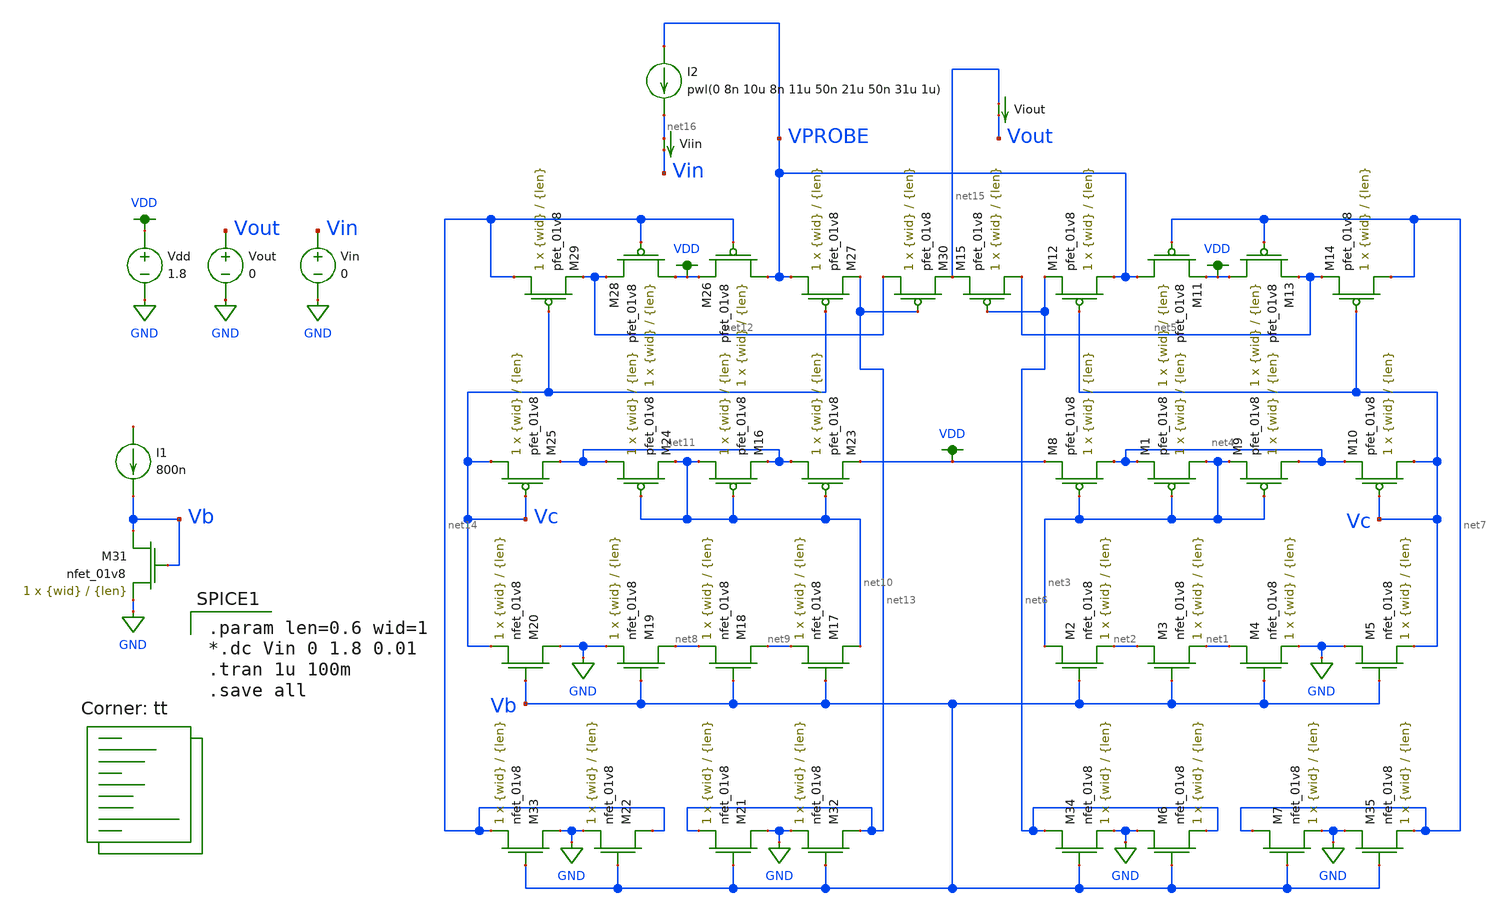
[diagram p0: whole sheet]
** sch_path: mp3/mirror_lvs_tb.sch
**.subckt mirror_lvs_tb
XM1 net3 net3 net4 VDD sky130_fd_pr__pfet_01v8 L={len} W={wid} nf=1 ad='int((nf+1)/2) * W/nf * 0.29'
+ as='int((nf+2)/2) * W/nf * 0.29' pd='2*int((nf+1)/2) * (W/nf + 0.29)' ps='2*int((nf+2)/2) * (W/nf + 0.29)'
+ nrd='0.29 / W' nrs='0.29 / W' sa=0 sb=0 sd=0 mult=1 m=1
XM2 net3 Vb net2 GND sky130_fd_pr__nfet_01v8 L={len} W={wid} nf=1 ad='int((nf+1)/2) * W/nf * 0.29' as='int((nf+2)/2) * W/nf * 0.29'
+ pd='2*int((nf+1)/2) * (W/nf + 0.29)' ps='2*int((nf+2)/2) * (W/nf + 0.29)' nrd='0.29 / W' nrs='0.29 / W'
+ sa=0 sb=0 sd=0 mult=1 m=1
XM3 net2 Vb net1 GND sky130_fd_pr__nfet_01v8 L={len} W={wid} nf=1 ad='int((nf+1)/2) * W/nf * 0.29' as='int((nf+2)/2) * W/nf * 0.29'
+ pd='2*int((nf+1)/2) * (W/nf + 0.29)' ps='2*int((nf+2)/2) * (W/nf + 0.29)' nrd='0.29 / W' nrs='0.29 / W'
+ sa=0 sb=0 sd=0 mult=1 m=1
XM4 net1 Vb GND GND sky130_fd_pr__nfet_01v8 L={len} W={wid} nf=1 ad='int((nf+1)/2) * W/nf * 0.29' as='int((nf+2)/2) * W/nf * 0.29'
+ pd='2*int((nf+1)/2) * (W/nf + 0.29)' ps='2*int((nf+2)/2) * (W/nf + 0.29)' nrd='0.29 / W' nrs='0.29 / W'
+ sa=0 sb=0 sd=0 mult=1 m=1
XM5 GND Vb Vc GND sky130_fd_pr__nfet_01v8 L={len} W={wid} nf=1 ad='int((nf+1)/2) * W/nf * 0.29' as='int((nf+2)/2) * W/nf * 0.29'
+ pd='2*int((nf+1)/2) * (W/nf + 0.29)' ps='2*int((nf+2)/2) * (W/nf + 0.29)' nrd='0.29 / W' nrs='0.29 / W'
+ sa=0 sb=0 sd=0 mult=1 m=1
XM8 net4 net3 VDD VDD sky130_fd_pr__pfet_01v8 L={len} W={wid} nf=1 ad='int((nf+1)/2) * W/nf * 0.29' as='int((nf+2)/2) * W/nf * 0.29'
+ pd='2*int((nf+1)/2) * (W/nf + 0.29)' ps='2*int((nf+2)/2) * (W/nf + 0.29)' nrd='0.29 / W' nrs='0.29 / W'
+ sa=0 sb=0 sd=0 mult=1 m=1
XM9 net4 net3 net3 VDD sky130_fd_pr__pfet_01v8 L={len} W={wid} nf=1 ad='int((nf+1)/2) * W/nf * 0.29'
+ as='int((nf+2)/2) * W/nf * 0.29' pd='2*int((nf+1)/2) * (W/nf + 0.29)' ps='2*int((nf+2)/2) * (W/nf + 0.29)'
+ nrd='0.29 / W' nrs='0.29 / W' sa=0 sb=0 sd=0 mult=1 m=1
XM10 Vc Vc net4 VDD sky130_fd_pr__pfet_01v8 L={len} W={wid} nf=1 ad='int((nf+1)/2) * W/nf * 0.29' as='int((nf+2)/2) * W/nf * 0.29'
+ pd='2*int((nf+1)/2) * (W/nf + 0.29)' ps='2*int((nf+2)/2) * (W/nf + 0.29)' nrd='0.29 / W' nrs='0.29 / W'
+ sa=0 sb=0 sd=0 mult=1 m=1
XM11 VPROBE net7 VDD VDD sky130_fd_pr__pfet_01v8 L={len} W={wid} nf=1 ad='int((nf+1)/2) * W/nf * 0.29'
+ as='int((nf+2)/2) * W/nf * 0.29' pd='2*int((nf+1)/2) * (W/nf + 0.29)' ps='2*int((nf+2)/2) * (W/nf + 0.29)'
+ nrd='0.29 / W' nrs='0.29 / W' sa=0 sb=0 sd=0 mult=1 m=1
XM12 VPROBE Vc net6 VDD sky130_fd_pr__pfet_01v8 L={len} W={wid} nf=1 ad='int((nf+1)/2) * W/nf * 0.29'
+ as='int((nf+2)/2) * W/nf * 0.29' pd='2*int((nf+1)/2) * (W/nf + 0.29)' ps='2*int((nf+2)/2) * (W/nf + 0.29)'
+ nrd='0.29 / W' nrs='0.29 / W' sa=0 sb=0 sd=0 mult=1 m=1
XM13 VDD net7 net5 VDD sky130_fd_pr__pfet_01v8 L={len} W={wid} nf=1 ad='int((nf+1)/2) * W/nf * 0.29'
+ as='int((nf+2)/2) * W/nf * 0.29' pd='2*int((nf+1)/2) * (W/nf + 0.29)' ps='2*int((nf+2)/2) * (W/nf + 0.29)'
+ nrd='0.29 / W' nrs='0.29 / W' sa=0 sb=0 sd=0 mult=1 m=1
XM14 net7 Vc net5 VDD sky130_fd_pr__pfet_01v8 L={len} W={wid} nf=1 ad='int((nf+1)/2) * W/nf * 0.29' as='int((nf+2)/2) * W/nf * 0.29'
+ pd='2*int((nf+1)/2) * (W/nf + 0.29)' ps='2*int((nf+2)/2) * (W/nf + 0.29)' nrd='0.29 / W' nrs='0.29 / W'
+ sa=0 sb=0 sd=0 mult=1 m=1
XM15 net5 net6 net15 VDD sky130_fd_pr__pfet_01v8 L={len} W={wid} nf=1 ad='int((nf+1)/2) * W/nf * 0.29'
+ as='int((nf+2)/2) * W/nf * 0.29' pd='2*int((nf+1)/2) * (W/nf + 0.29)' ps='2*int((nf+2)/2) * (W/nf + 0.29)'
+ nrd='0.29 / W' nrs='0.29 / W' sa=0 sb=0 sd=0 mult=1 m=1
XM16 net10 net10 net11 VDD sky130_fd_pr__pfet_01v8 L={len} W={wid} nf=1 ad='int((nf+1)/2) * W/nf * 0.29'
+ as='int((nf+2)/2) * W/nf * 0.29' pd='2*int((nf+1)/2) * (W/nf + 0.29)' ps='2*int((nf+2)/2) * (W/nf + 0.29)'
+ nrd='0.29 / W' nrs='0.29 / W' sa=0 sb=0 sd=0 mult=1 m=1
XM17 net10 Vb net9 GND sky130_fd_pr__nfet_01v8 L={len} W={wid} nf=1 ad='int((nf+1)/2) * W/nf * 0.29'
+ as='int((nf+2)/2) * W/nf * 0.29' pd='2*int((nf+1)/2) * (W/nf + 0.29)' ps='2*int((nf+2)/2) * (W/nf + 0.29)'
+ nrd='0.29 / W' nrs='0.29 / W' sa=0 sb=0 sd=0 mult=1 m=1
XM18 net9 Vb net8 GND sky130_fd_pr__nfet_01v8 L={len} W={wid} nf=1 ad='int((nf+1)/2) * W/nf * 0.29' as='int((nf+2)/2) * W/nf * 0.29'
+ pd='2*int((nf+1)/2) * (W/nf + 0.29)' ps='2*int((nf+2)/2) * (W/nf + 0.29)' nrd='0.29 / W' nrs='0.29 / W'
+ sa=0 sb=0 sd=0 mult=1 m=1
XM19 net8 Vb GND GND sky130_fd_pr__nfet_01v8 L={len} W={wid} nf=1 ad='int((nf+1)/2) * W/nf * 0.29' as='int((nf+2)/2) * W/nf * 0.29'
+ pd='2*int((nf+1)/2) * (W/nf + 0.29)' ps='2*int((nf+2)/2) * (W/nf + 0.29)' nrd='0.29 / W' nrs='0.29 / W'
+ sa=0 sb=0 sd=0 mult=1 m=1
XM20 GND Vb Vc GND sky130_fd_pr__nfet_01v8 L={len} W={wid} nf=1 ad='int((nf+1)/2) * W/nf * 0.29' as='int((nf+2)/2) * W/nf * 0.29'
+ pd='2*int((nf+1)/2) * (W/nf + 0.29)' ps='2*int((nf+2)/2) * (W/nf + 0.29)' nrd='0.29 / W' nrs='0.29 / W'
+ sa=0 sb=0 sd=0 mult=1 m=1
XM21 GND Vb net13 GND sky130_fd_pr__nfet_01v8 L={len} W={wid} nf=1 ad='int((nf+1)/2) * W/nf * 0.29' as='int((nf+2)/2) * W/nf * 0.29'
+ pd='2*int((nf+1)/2) * (W/nf + 0.29)' ps='2*int((nf+2)/2) * (W/nf + 0.29)' nrd='0.29 / W' nrs='0.29 / W'
+ sa=0 sb=0 sd=0 mult=1 m=1
XM22 net14 Vb GND GND sky130_fd_pr__nfet_01v8 L={len} W={wid} nf=1 ad='int((nf+1)/2) * W/nf * 0.29' as='int((nf+2)/2) * W/nf * 0.29'
+ pd='2*int((nf+1)/2) * (W/nf + 0.29)' ps='2*int((nf+2)/2) * (W/nf + 0.29)' nrd='0.29 / W' nrs='0.29 / W'
+ sa=0 sb=0 sd=0 mult=1 m=1
XM23 net11 net10 VDD VDD sky130_fd_pr__pfet_01v8 L={len} W={wid} nf=1 ad='int((nf+1)/2) * W/nf * 0.29'
+ as='int((nf+2)/2) * W/nf * 0.29' pd='2*int((nf+1)/2) * (W/nf + 0.29)' ps='2*int((nf+2)/2) * (W/nf + 0.29)'
+ nrd='0.29 / W' nrs='0.29 / W' sa=0 sb=0 sd=0 mult=1 m=1
XM24 net11 net10 net10 VDD sky130_fd_pr__pfet_01v8 L={len} W={wid} nf=1 ad='int((nf+1)/2) * W/nf * 0.29'
+ as='int((nf+2)/2) * W/nf * 0.29' pd='2*int((nf+1)/2) * (W/nf + 0.29)' ps='2*int((nf+2)/2) * (W/nf + 0.29)'
+ nrd='0.29 / W' nrs='0.29 / W' sa=0 sb=0 sd=0 mult=1 m=1
XM25 Vc Vc net11 VDD sky130_fd_pr__pfet_01v8 L={len} W={wid} nf=1 ad='int((nf+1)/2) * W/nf * 0.29' as='int((nf+2)/2) * W/nf * 0.29'
+ pd='2*int((nf+1)/2) * (W/nf + 0.29)' ps='2*int((nf+2)/2) * (W/nf + 0.29)' nrd='0.29 / W' nrs='0.29 / W'
+ sa=0 sb=0 sd=0 mult=1 m=1
XM26 VPROBE net14 VDD VDD sky130_fd_pr__pfet_01v8 L={len} W={wid} nf=1 ad='int((nf+1)/2) * W/nf * 0.29'
+ as='int((nf+2)/2) * W/nf * 0.29' pd='2*int((nf+1)/2) * (W/nf + 0.29)' ps='2*int((nf+2)/2) * (W/nf + 0.29)'
+ nrd='0.29 / W' nrs='0.29 / W' sa=0 sb=0 sd=0 mult=1 m=1
XM27 VPROBE Vc net13 VDD sky130_fd_pr__pfet_01v8 L={len} W={wid} nf=1 ad='int((nf+1)/2) * W/nf * 0.29'
+ as='int((nf+2)/2) * W/nf * 0.29' pd='2*int((nf+1)/2) * (W/nf + 0.29)' ps='2*int((nf+2)/2) * (W/nf + 0.29)'
+ nrd='0.29 / W' nrs='0.29 / W' sa=0 sb=0 sd=0 mult=1 m=1
XM28 VDD net14 net12 VDD sky130_fd_pr__pfet_01v8 L={len} W={wid} nf=1 ad='int((nf+1)/2) * W/nf * 0.29'
+ as='int((nf+2)/2) * W/nf * 0.29' pd='2*int((nf+1)/2) * (W/nf + 0.29)' ps='2*int((nf+2)/2) * (W/nf + 0.29)'
+ nrd='0.29 / W' nrs='0.29 / W' sa=0 sb=0 sd=0 mult=1 m=1
XM29 net14 Vc net12 VDD sky130_fd_pr__pfet_01v8 L={len} W={wid} nf=1 ad='int((nf+1)/2) * W/nf * 0.29'
+ as='int((nf+2)/2) * W/nf * 0.29' pd='2*int((nf+1)/2) * (W/nf + 0.29)' ps='2*int((nf+2)/2) * (W/nf + 0.29)'
+ nrd='0.29 / W' nrs='0.29 / W' sa=0 sb=0 sd=0 mult=1 m=1
XM30 net12 net13 net15 VDD sky130_fd_pr__pfet_01v8 L={len} W={wid} nf=1 ad='int((nf+1)/2) * W/nf * 0.29'
+ as='int((nf+2)/2) * W/nf * 0.29' pd='2*int((nf+1)/2) * (W/nf + 0.29)' ps='2*int((nf+2)/2) * (W/nf + 0.29)'
+ nrd='0.29 / W' nrs='0.29 / W' sa=0 sb=0 sd=0 mult=1 m=1
Vdd VDD GND 1.8
I1 net17 Vb 800n
XM31 Vb Vb GND GND sky130_fd_pr__nfet_01v8 L={len} W={wid} nf=1 ad='int((nf+1)/2) * W/nf * 0.29' as='int((nf+2)/2) * W/nf * 0.29'
+ pd='2*int((nf+1)/2) * (W/nf + 0.29)' ps='2*int((nf+2)/2) * (W/nf + 0.29)' nrd='0.29 / W' nrs='0.29 / W'
+ sa=0 sb=0 sd=0 mult=1 m=1
I2 VPROBE net16 pwl(0 8n 10u 8n 11u 50n 21u 50n 31u 1u)
Vout Vout GND 0
Viout net15 Vout 0
.save i(viout)
Viin net16 Vin 0
.save i(viin)
Vin Vin GND 0
XM32 net13 Vb GND GND sky130_fd_pr__nfet_01v8 L={len} W={wid} nf=1 ad='int((nf+1)/2) * W/nf * 0.29' as='int((nf+2)/2) * W/nf * 0.29'
+ pd='2*int((nf+1)/2) * (W/nf + 0.29)' ps='2*int((nf+2)/2) * (W/nf + 0.29)' nrd='0.29 / W' nrs='0.29 / W'
+ sa=0 sb=0 sd=0 mult=1 m=1
XM33 GND Vb net14 GND sky130_fd_pr__nfet_01v8 L={len} W={wid} nf=1 ad='int((nf+1)/2) * W/nf * 0.29' as='int((nf+2)/2) * W/nf * 0.29'
+ pd='2*int((nf+1)/2) * (W/nf + 0.29)' ps='2*int((nf+2)/2) * (W/nf + 0.29)' nrd='0.29 / W' nrs='0.29 / W'
+ sa=0 sb=0 sd=0 mult=1 m=1
XM6 GND Vb net6 GND sky130_fd_pr__nfet_01v8 L={len} W={wid} nf=1 ad='int((nf+1)/2) * W/nf * 0.29' as='int((nf+2)/2) * W/nf * 0.29'
+ pd='2*int((nf+1)/2) * (W/nf + 0.29)' ps='2*int((nf+2)/2) * (W/nf + 0.29)' nrd='0.29 / W' nrs='0.29 / W'
+ sa=0 sb=0 sd=0 mult=1 m=1
XM7 net7 Vb GND GND sky130_fd_pr__nfet_01v8 L={len} W={wid} nf=1 ad='int((nf+1)/2) * W/nf * 0.29' as='int((nf+2)/2) * W/nf * 0.29'
+ pd='2*int((nf+1)/2) * (W/nf + 0.29)' ps='2*int((nf+2)/2) * (W/nf + 0.29)' nrd='0.29 / W' nrs='0.29 / W'
+ sa=0 sb=0 sd=0 mult=1 m=1
XM34 net6 Vb GND GND sky130_fd_pr__nfet_01v8 L={len} W={wid} nf=1 ad='int((nf+1)/2) * W/nf * 0.29' as='int((nf+2)/2) * W/nf * 0.29'
+ pd='2*int((nf+1)/2) * (W/nf + 0.29)' ps='2*int((nf+2)/2) * (W/nf + 0.29)' nrd='0.29 / W' nrs='0.29 / W'
+ sa=0 sb=0 sd=0 mult=1 m=1
XM35 GND Vb net7 GND sky130_fd_pr__nfet_01v8 L={len} W={wid} nf=1 ad='int((nf+1)/2) * W/nf * 0.29' as='int((nf+2)/2) * W/nf * 0.29'
+ pd='2*int((nf+1)/2) * (W/nf + 0.29)' ps='2*int((nf+2)/2) * (W/nf + 0.29)' nrd='0.29 / W' nrs='0.29 / W'
+ sa=0 sb=0 sd=0 mult=1 m=1
**** begin user architecture code
.lib $::SKYWATER_MODELS/sky130.lib.spice tt

.param len=0.6 wid=1
*.dc Vin 0 1.8 0.01
.tran 1u 100m
.save all


**** end user architecture code
**.ends
.GLOBAL GND
.GLOBAL VDD
.end
